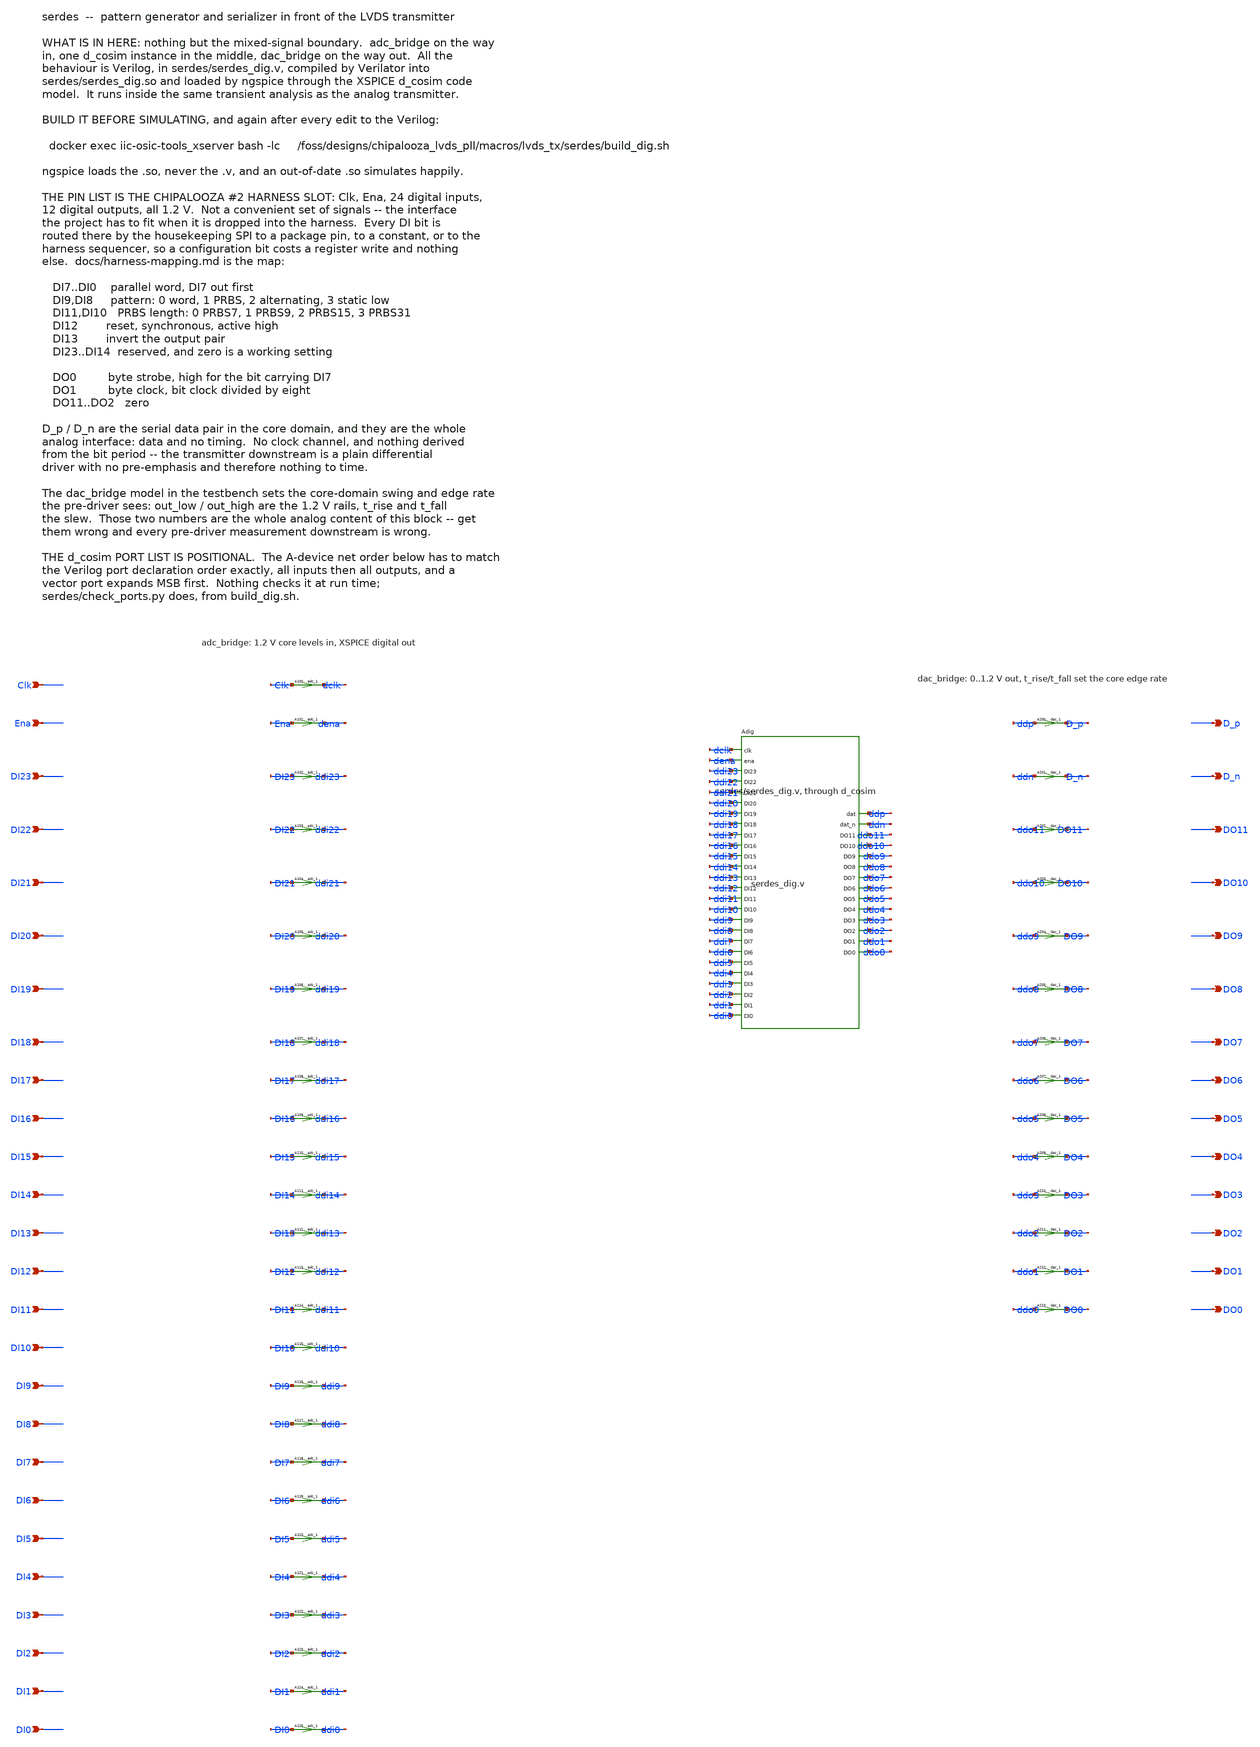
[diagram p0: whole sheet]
** sch_path: macros/lvds_tx/schematic/xschem/serdes.sch
**.subckt serdes Clk Ena DI23 DI22 DI21 DI20 DI19 DI18 DI17 DI16 DI15 DI14 DI13 DI12 DI11 DI10 DI9
*+ DI8 DI7 DI6 DI5 DI4 DI3 DI2 DI1 DI0 D_p D_n DO11 DO10 DO9 DO8 DO7 DO6 DO5 DO4 DO3 DO2 DO1 DO0
*.ipin Clk
*.ipin Ena
*.ipin DI23
*.ipin DI22
*.ipin DI21
*.ipin DI20
*.ipin DI19
*.ipin DI18
*.ipin DI17
*.ipin DI16
*.ipin DI15
*.ipin DI14
*.ipin DI13
*.ipin DI12
*.ipin DI11
*.ipin DI10
*.ipin DI9
*.ipin DI8
*.ipin DI7
*.ipin DI6
*.ipin DI5
*.ipin DI4
*.ipin DI3
*.ipin DI2
*.ipin DI1
*.ipin DI0
*.opin D_p
*.opin D_n
*.opin DO11
*.opin DO10
*.opin DO9
*.opin DO8
*.opin DO7
*.opin DO6
*.opin DO5
*.opin DO4
*.opin DO3
*.opin DO2
*.opin DO1
*.opin DO0
A100 [ Clk ] [ dclk ] adc_1
A101 [ Ena ] [ dena ] adc_1
A102 [ DI23 ] [ ddi23 ] adc_1
A103 [ DI22 ] [ ddi22 ] adc_1
A104 [ DI21 ] [ ddi21 ] adc_1
A105 [ DI20 ] [ ddi20 ] adc_1
A106 [ DI19 ] [ ddi19 ] adc_1
A107 [ DI18 ] [ ddi18 ] adc_1
A108 [ DI17 ] [ ddi17 ] adc_1
A109 [ DI16 ] [ ddi16 ] adc_1
A110 [ DI15 ] [ ddi15 ] adc_1
A111 [ DI14 ] [ ddi14 ] adc_1
A112 [ DI13 ] [ ddi13 ] adc_1
A113 [ DI12 ] [ ddi12 ] adc_1
A114 [ DI11 ] [ ddi11 ] adc_1
A115 [ DI10 ] [ ddi10 ] adc_1
A116 [ DI9 ] [ ddi9 ] adc_1
A117 [ DI8 ] [ ddi8 ] adc_1
A118 [ DI7 ] [ ddi7 ] adc_1
A119 [ DI6 ] [ ddi6 ] adc_1
A120 [ DI5 ] [ ddi5 ] adc_1
A121 [ DI4 ] [ ddi4 ] adc_1
A122 [ DI3 ] [ ddi3 ] adc_1
A123 [ DI2 ] [ ddi2 ] adc_1
A124 [ DI1 ] [ ddi1 ] adc_1
A125 [ DI0 ] [ ddi0 ] adc_1
Adig [ dclk dena ddi23 ddi22 ddi21 ddi20 ddi19 ddi18 ddi17 ddi16 ddi15 ddi14 ddi13 ddi12 ddi11 ddi10
+ ddi9 ddi8 ddi7 ddi6 ddi5 ddi4 ddi3 ddi2 ddi1 ddi0 ] [ ddp ddn ddo11 ddo10 ddo9 ddo8 ddo7 ddo6 ddo5 ddo4
+ ddo3 ddo2 ddo1 ddo0 ] serdes_dig_1
A200 [ ddp ] [ D_p ] dac_1
A201 [ ddn ] [ D_n ] dac_1
A202 [ ddo11 ] [ DO11 ] dac_1
A203 [ ddo10 ] [ DO10 ] dac_1
A204 [ ddo9 ] [ DO9 ] dac_1
A205 [ ddo8 ] [ DO8 ] dac_1
A206 [ ddo7 ] [ DO7 ] dac_1
A207 [ ddo6 ] [ DO6 ] dac_1
A208 [ ddo5 ] [ DO5 ] dac_1
A209 [ ddo4 ] [ DO4 ] dac_1
A210 [ ddo3 ] [ DO3 ] dac_1
A211 [ ddo2 ] [ DO2 ] dac_1
A212 [ ddo1 ] [ DO1 ] dac_1
A213 [ ddo0 ] [ DO0 ] dac_1
**.ends
.end
